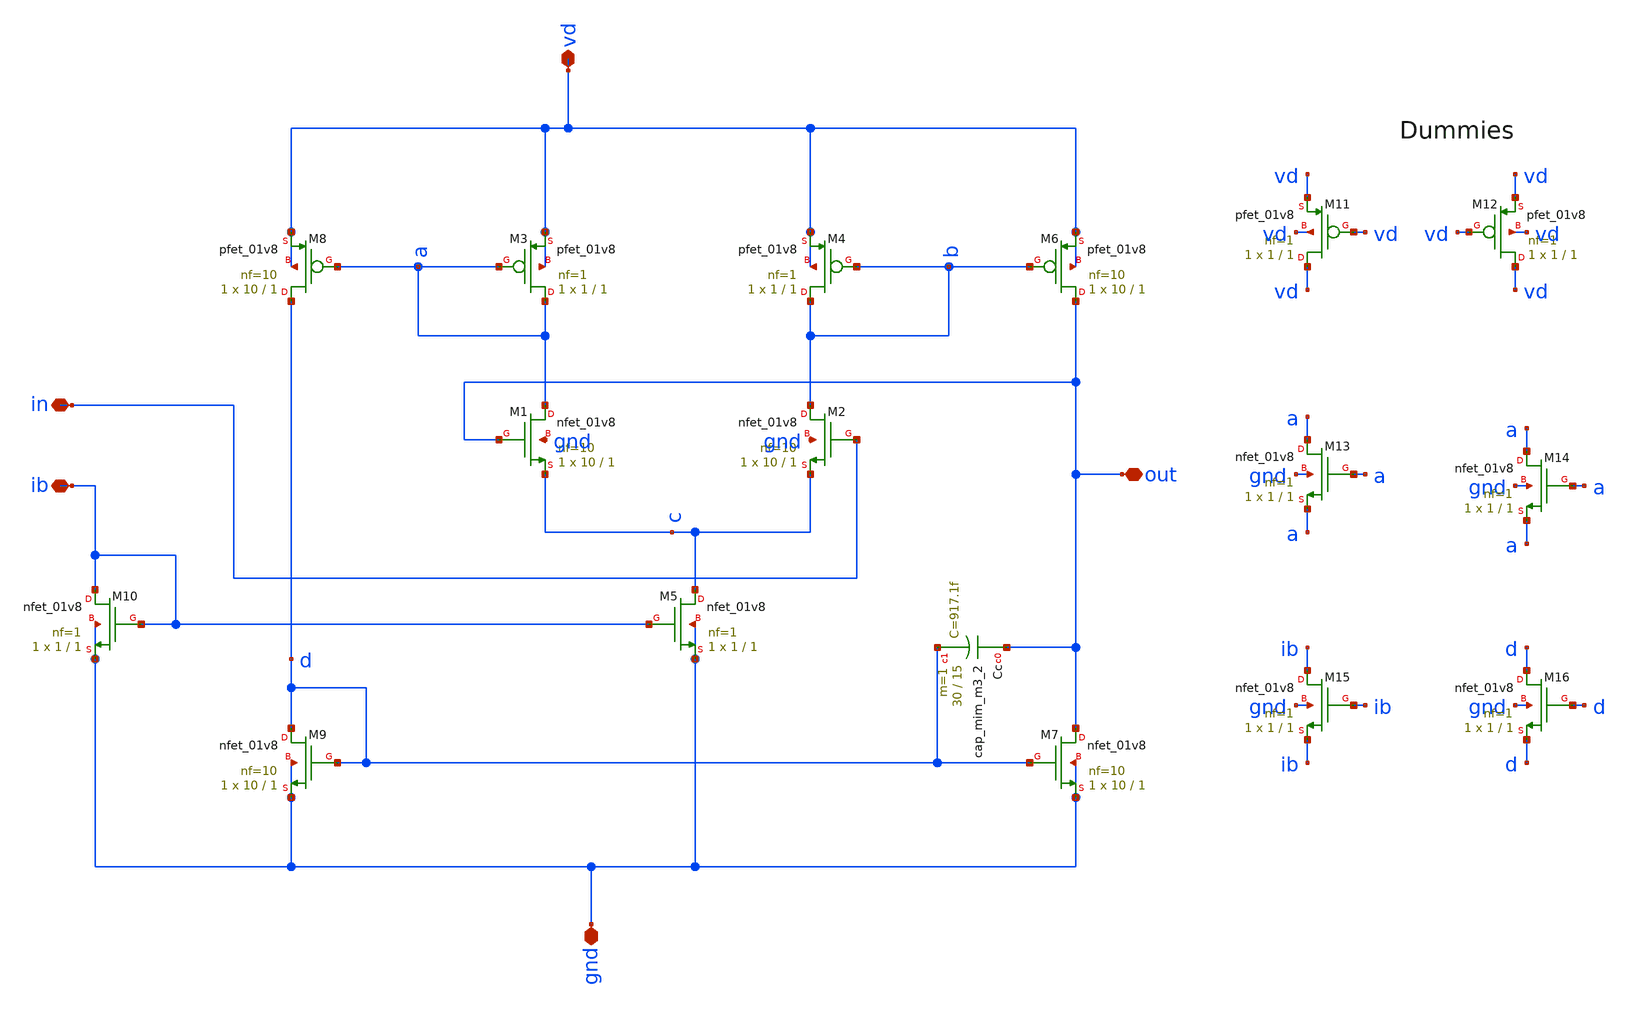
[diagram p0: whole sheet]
** sch_path: buffer/xschem/buffer.sch
* Copyright 2020 Stefan Frederik Schippers
* Licensed under the Apache License, Version 2.0 (the "License");
* you may not use this file except in compliance with the License.
* You may obtain a copy of the License at
* https://www.apache.org/licenses/LICENSE-2.0
* Unless required by applicable law or agreed to in writing, software
* distributed under the License is distributed on an "AS IS" BASIS,
* WITHOUT WARRANTIES OR CONDITIONS OF ANY KIND, either express or implied.
* See the License for the specific language governing permissions and
* limitations under the License.
**.subckt buffer vd ib out in gnd
*.iopin vd
*.iopin ib
*.iopin out
*.iopin in
*.iopin gnd
XM3 a a vd vd sky130_fd_pr__pfet_01v8 L=1 W=1 nf=1 ad='int((nf+1)/2) * W/nf * 0.29' as='int((nf+2)/2) * W/nf * 0.29'
+ pd='2*int((nf+1)/2) * (W/nf + 0.29)' ps='2*int((nf+2)/2) * (W/nf + 0.29)' nrd='0.29 / W' nrs='0.29 / W'
+ sa=0 sb=0 sd=0 mult=1 m=1
XM1 a out c gnd sky130_fd_pr__nfet_01v8 L=1 W=10 nf=10 ad='int((nf+1)/2) * W/nf * 0.29' as='int((nf+2)/2) * W/nf * 0.29'
+ pd='2*int((nf+1)/2) * (W/nf + 0.29)' ps='2*int((nf+2)/2) * (W/nf + 0.29)' nrd='0.29 / W' nrs='0.29 / W'
+ sa=0 sb=0 sd=0 mult=1 m=1
XM2 b in c gnd sky130_fd_pr__nfet_01v8 L=1 W=10 nf=10 ad='int((nf+1)/2) * W/nf * 0.29' as='int((nf+2)/2) * W/nf * 0.29'
+ pd='2*int((nf+1)/2) * (W/nf + 0.29)' ps='2*int((nf+2)/2) * (W/nf + 0.29)' nrd='0.29 / W' nrs='0.29 / W'
+ sa=0 sb=0 sd=0 mult=1 m=1
XM4 b b vd vd sky130_fd_pr__pfet_01v8 L=1 W=1 nf=1 ad='int((nf+1)/2) * W/nf * 0.29' as='int((nf+2)/2) * W/nf * 0.29'
+ pd='2*int((nf+1)/2) * (W/nf + 0.29)' ps='2*int((nf+2)/2) * (W/nf + 0.29)' nrd='0.29 / W' nrs='0.29 / W'
+ sa=0 sb=0 sd=0 mult=1 m=1
XM5 c ib gnd gnd sky130_fd_pr__nfet_01v8 L=1 W=1 nf=1 ad='int((nf+1)/2) * W/nf * 0.29' as='int((nf+2)/2) * W/nf * 0.29'
+ pd='2*int((nf+1)/2) * (W/nf + 0.29)' ps='2*int((nf+2)/2) * (W/nf + 0.29)' nrd='0.29 / W' nrs='0.29 / W'
+ sa=0 sb=0 sd=0 mult=1 m=1
XM6 out b vd vd sky130_fd_pr__pfet_01v8 L=1 W=10 nf=10 ad='int((nf+1)/2) * W/nf * 0.29' as='int((nf+2)/2) * W/nf * 0.29'
+ pd='2*int((nf+1)/2) * (W/nf + 0.29)' ps='2*int((nf+2)/2) * (W/nf + 0.29)' nrd='0.29 / W' nrs='0.29 / W'
+ sa=0 sb=0 sd=0 mult=1 m=1
XM7 out d gnd gnd sky130_fd_pr__nfet_01v8 L=1 W=10 nf=10 ad='int((nf+1)/2) * W/nf * 0.29' as='int((nf+2)/2) * W/nf * 0.29'
+ pd='2*int((nf+1)/2) * (W/nf + 0.29)' ps='2*int((nf+2)/2) * (W/nf + 0.29)' nrd='0.29 / W' nrs='0.29 / W'
+ sa=0 sb=0 sd=0 mult=1 m=1
XM8 d a vd vd sky130_fd_pr__pfet_01v8 L=1 W=10 nf=10 ad='int((nf+1)/2) * W/nf * 0.29' as='int((nf+2)/2) * W/nf * 0.29'
+ pd='2*int((nf+1)/2) * (W/nf + 0.29)' ps='2*int((nf+2)/2) * (W/nf + 0.29)' nrd='0.29 / W' nrs='0.29 / W'
+ sa=0 sb=0 sd=0 mult=1 m=1
XM9 d d gnd gnd sky130_fd_pr__nfet_01v8 L=1 W=10 nf=10 ad='int((nf+1)/2) * W/nf * 0.29' as='int((nf+2)/2) * W/nf * 0.29'
+ pd='2*int((nf+1)/2) * (W/nf + 0.29)' ps='2*int((nf+2)/2) * (W/nf + 0.29)' nrd='0.29 / W' nrs='0.29 / W'
+ sa=0 sb=0 sd=0 mult=1 m=1
XM10 ib ib gnd gnd sky130_fd_pr__nfet_01v8 L=1 W=1 nf=1 ad='int((nf+1)/2) * W/nf * 0.29' as='int((nf+2)/2) * W/nf * 0.29'
+ pd='2*int((nf+1)/2) * (W/nf + 0.29)' ps='2*int((nf+2)/2) * (W/nf + 0.29)' nrd='0.29 / W' nrs='0.29 / W'
+ sa=0 sb=0 sd=0 mult=1 m=1
XCc out d sky130_fd_pr__cap_mim_m3_2 W=30 L=15 MF=1 m=1
XM11 vd vd vd vd sky130_fd_pr__pfet_01v8 L=1 W=1 nf=1 ad='int((nf+1)/2) * W/nf * 0.29' as='int((nf+2)/2) * W/nf * 0.29'
+ pd='2*int((nf+1)/2) * (W/nf + 0.29)' ps='2*int((nf+2)/2) * (W/nf + 0.29)' nrd='0.29 / W' nrs='0.29 / W'
+ sa=0 sb=0 sd=0 mult=1 m=1
XM12 vd vd vd vd sky130_fd_pr__pfet_01v8 L=1 W=1 nf=1 ad='int((nf+1)/2) * W/nf * 0.29' as='int((nf+2)/2) * W/nf * 0.29'
+ pd='2*int((nf+1)/2) * (W/nf + 0.29)' ps='2*int((nf+2)/2) * (W/nf + 0.29)' nrd='0.29 / W' nrs='0.29 / W'
+ sa=0 sb=0 sd=0 mult=1 m=1
XM13 a a a gnd sky130_fd_pr__nfet_01v8 L=1 W=1 nf=1 ad='int((nf+1)/2) * W/nf * 0.29' as='int((nf+2)/2) * W/nf * 0.29'
+ pd='2*int((nf+1)/2) * (W/nf + 0.29)' ps='2*int((nf+2)/2) * (W/nf + 0.29)' nrd='0.29 / W' nrs='0.29 / W'
+ sa=0 sb=0 sd=0 mult=1 m=1
XM14 a a a gnd sky130_fd_pr__nfet_01v8 L=1 W=1 nf=1 ad='int((nf+1)/2) * W/nf * 0.29' as='int((nf+2)/2) * W/nf * 0.29'
+ pd='2*int((nf+1)/2) * (W/nf + 0.29)' ps='2*int((nf+2)/2) * (W/nf + 0.29)' nrd='0.29 / W' nrs='0.29 / W'
+ sa=0 sb=0 sd=0 mult=1 m=1
XM15 ib ib ib gnd sky130_fd_pr__nfet_01v8 L=1 W=1 nf=1 ad='int((nf+1)/2) * W/nf * 0.29' as='int((nf+2)/2) * W/nf * 0.29'
+ pd='2*int((nf+1)/2) * (W/nf + 0.29)' ps='2*int((nf+2)/2) * (W/nf + 0.29)' nrd='0.29 / W' nrs='0.29 / W'
+ sa=0 sb=0 sd=0 mult=1 m=1
XM16 d d d gnd sky130_fd_pr__nfet_01v8 L=1 W=1 nf=1 ad='int((nf+1)/2) * W/nf * 0.29' as='int((nf+2)/2) * W/nf * 0.29'
+ pd='2*int((nf+1)/2) * (W/nf + 0.29)' ps='2*int((nf+2)/2) * (W/nf + 0.29)' nrd='0.29 / W' nrs='0.29 / W'
+ sa=0 sb=0 sd=0 mult=1 m=1
**.ends
.end
